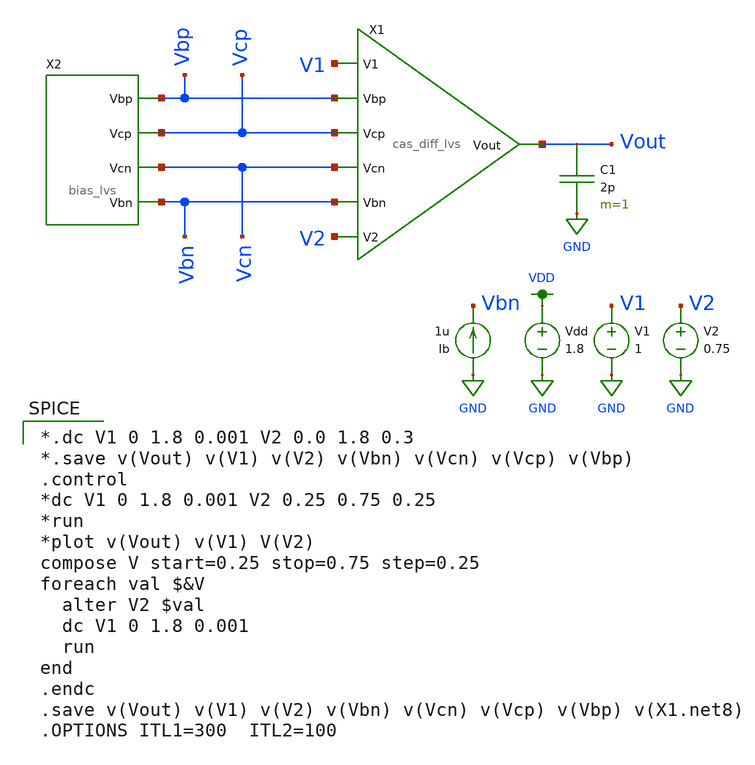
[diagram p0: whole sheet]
** sch_path: mini3/schem/vtc_noninv.sch
**.subckt vtc_noninv
X1 V1 V2 Vout Vbp Vcp Vcn Vbn cas_diff_lvs
Vdd VDD GND 1.8
V1 V1 GND 1
V2 V2 GND 0.75
Ib GND Vbn 1u
C1 Vout GND 2p m=1
X2 Vbp Vcp Vcn Vbn bias_lvs
**** begin user architecture code

.option wnflag=1
.lib ~/skywater/skywater-pdk/libraries/sky130_fd_pr_ngspice/latest/models/sky130.lib.spice tt


*.dc V1 0 1.8 0.001 V2 0.0 1.8 0.3
*.save v(Vout) v(V1) v(V2) v(Vbn) v(Vcn) v(Vcp) v(Vbp)
.control
*dc V1 0 1.8 0.001 V2 0.25 0.75 0.25
*run
*plot v(Vout) v(V1) V(V2)
compose V start=0.25 stop=0.75 step=0.25
foreach val $&V
  alter V2 $val
  dc V1 0 1.8 0.001
  run
end
.endc
.save v(Vout) v(V1) v(V2) v(Vbn) v(Vcn) v(Vcp) v(Vbp) v(X1.net8)
.OPTIONS ITL1=300  ITL2=100

**** end user architecture code
**.ends
.GLOBAL VDD
.GLOBAL GND
.end
